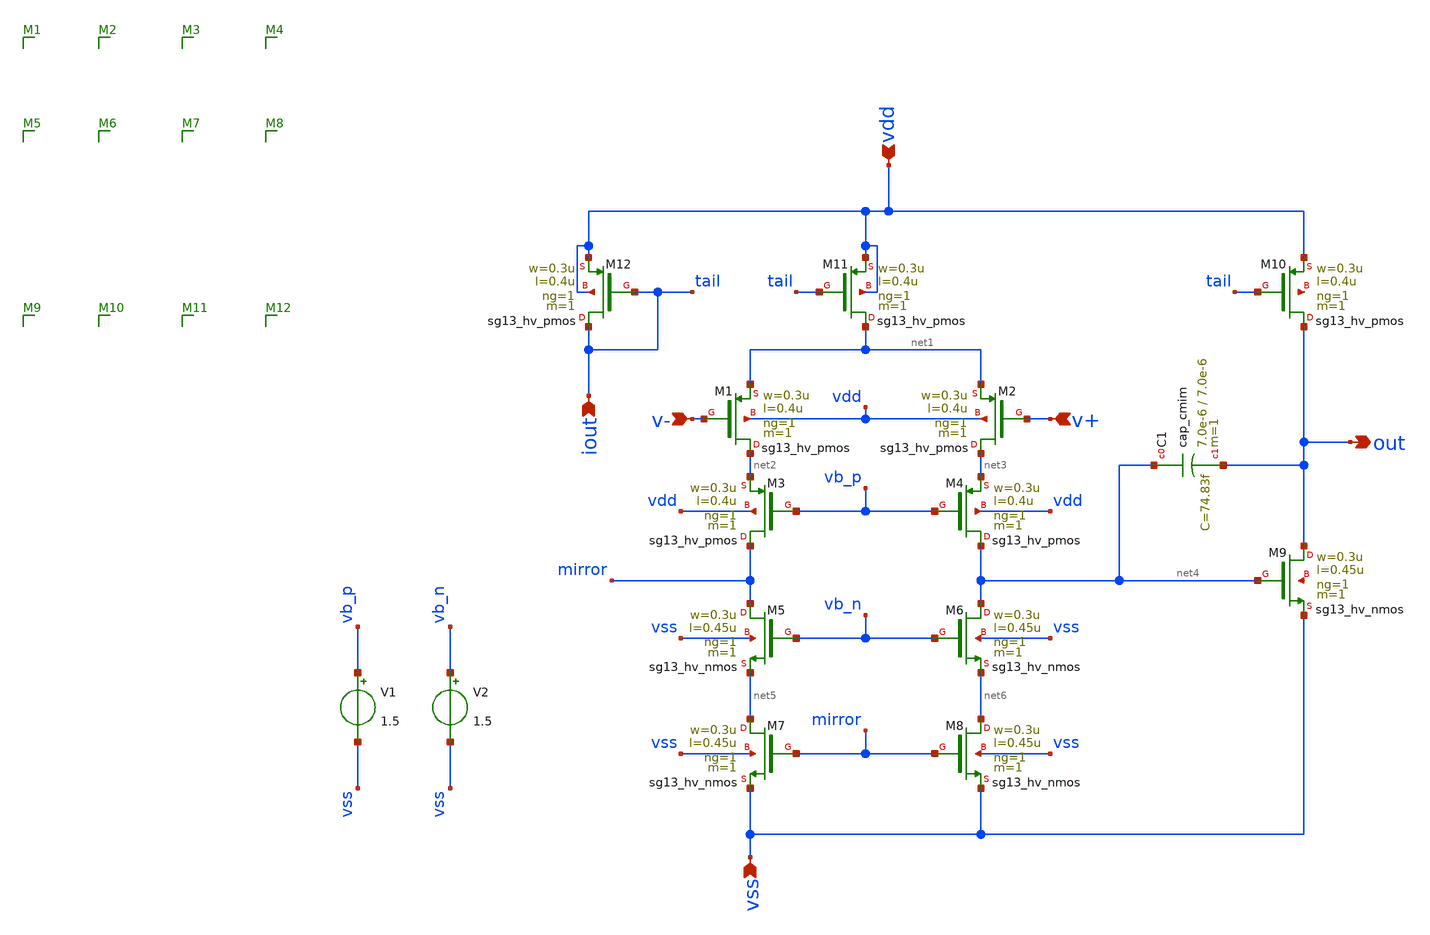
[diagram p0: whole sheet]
** sch_path: schematic/two_stage.sch
**.subckt two_stage out iout v- v+ vdd vss
*.opin out
*.ipin iout
*.ipin v-
*.ipin v+
*.ipin vdd
*.ipin vss
XM1 net2 v- net1 vdd sg13_hv_pmos w=0.3u l=0.4u ng=1 m=1 mm_ok=1
XM2 net3 v+ net1 vdd sg13_hv_pmos w=0.3u l=0.4u ng=1 m=1 mm_ok=1
XM5 mirror vb_n net5 vss sg13_hv_nmos w=0.3u l=0.45u ng=1 m=1 mm_ok=1
XM11 net1 tail vdd vdd sg13_hv_pmos w=0.3u l=0.4u ng=1 m=1 mm_ok=1
XM12 tail tail vdd vdd sg13_hv_pmos w=0.3u l=0.4u ng=1 m=1 mm_ok=1
XM3 mirror vb_p net2 vdd sg13_hv_pmos w=0.3u l=0.4u ng=1 m=1 mm_ok=1
XM4 net4 vb_p net3 vdd sg13_hv_pmos w=0.3u l=0.4u ng=1 m=1 mm_ok=1
XM6 net4 vb_n net6 vss sg13_hv_nmos w=0.3u l=0.45u ng=1 m=1 mm_ok=1
XM7 net5 mirror vss vss sg13_hv_nmos w=0.3u l=0.45u ng=1 m=1 mm_ok=1
XM8 net6 mirror vss vss sg13_hv_nmos w=0.3u l=0.45u ng=1 m=1 mm_ok=1
XM9 out net4 vss net7 sg13_hv_nmos w=0.3u l=0.45u ng=1 m=1 mm_ok=1
XC1 net4 out cap_cmim w=7.0e-6 l=7.0e-6 m=1 mm_ok=1
XM10 out tail vdd net8 sg13_hv_pmos w=0.3u l=0.4u ng=1 m=1 mm_ok=1
V1 vb_p vss 1.5
V2 vb_n vss 1.5
**.ends
.end
